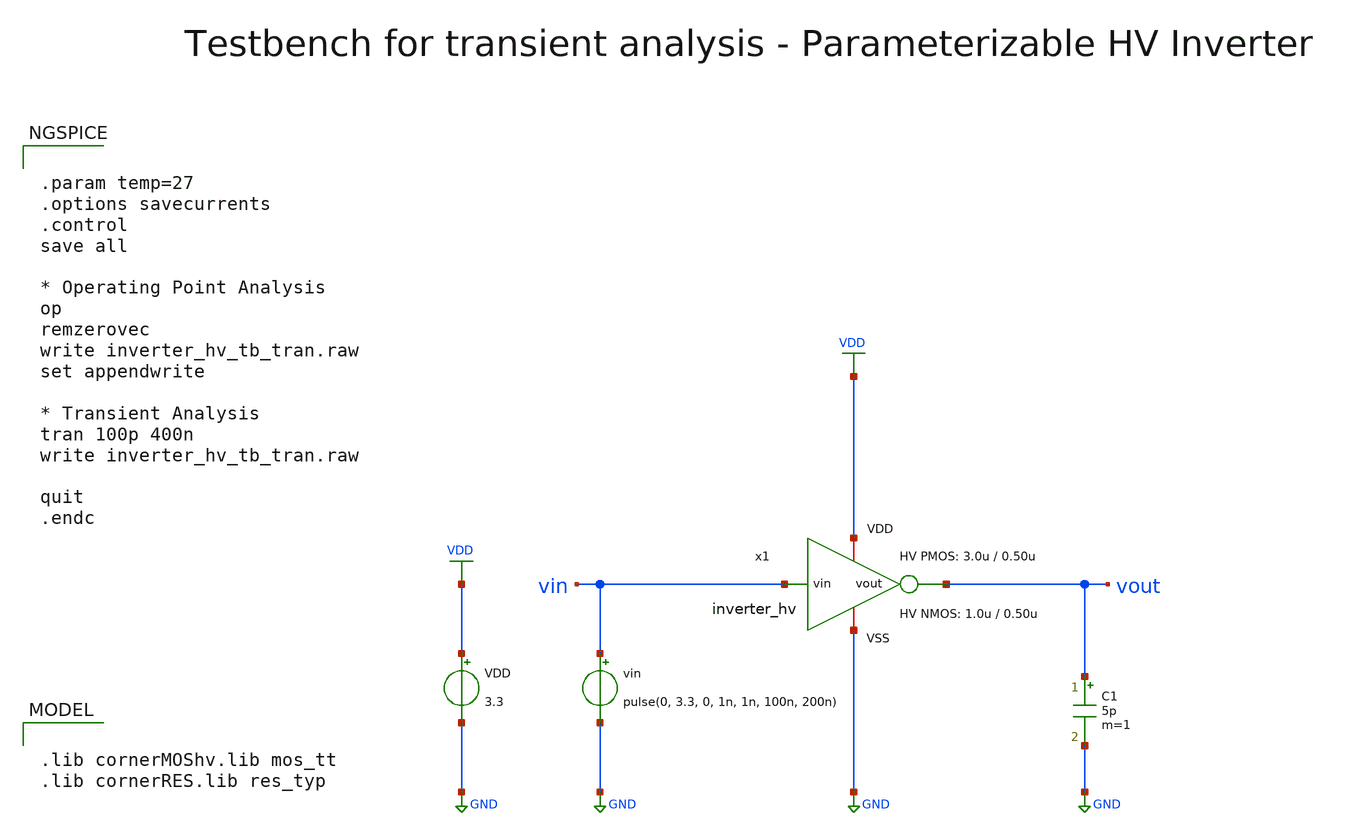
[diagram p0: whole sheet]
** sch_path: SG13G2_ATBS-ADC-main/xschem/inverter/testbenches/inverter_hv_tb_tran.sch
**.subckt inverter_hv_tb_tran
VDD VDD GND 3.3
vin vin GND pulse(0, 3.3, 0, 1n, 1n, 100n, 200n)
C1 vout GND 5p m=1
x1 VDD vin vout GND inverter_hv W_P=3.0u L_P=0.50u W_N=1.0u L_N=0.50u
**** begin user architecture code

.lib cornerMOShv.lib mos_tt
.lib cornerRES.lib res_typ



.param temp=27
.options savecurrents
.control
save all

* Operating Point Analysis
op
remzerovec
write inverter_hv_tb_tran.raw
set appendwrite

* Transient Analysis
tran 100p 400n
write inverter_hv_tb_tran.raw

quit
.endc


**** end user architecture code
**.ends

* expanding   symbol:  inverter/inverter_hv.sym # of pins=4
** sym_path: SG13G2_ATBS-ADC-main/xschem/inverter/inverter_hv.sym
** sch_path: SG13G2_ATBS-ADC-main/xschem/inverter/inverter_hv.sch
.subckt inverter_hv VDD vin vout VSS  W_P=3.0u L_P=0.50u W_N=1.0u L_N=0.50u
*.ipin vin
*.iopin VDD
*.iopin VSS
*.opin vout
XM1 vout vin VDD VDD sg13_hv_pmos w=W_P l=L_P ng=1 m=1 mm_ok=1
XM2 vout vin VSS VSS sg13_hv_nmos w=W_N l=L_N ng=1 m=1 mm_ok=1
.ends

.GLOBAL GND
.GLOBAL VDD
.end
